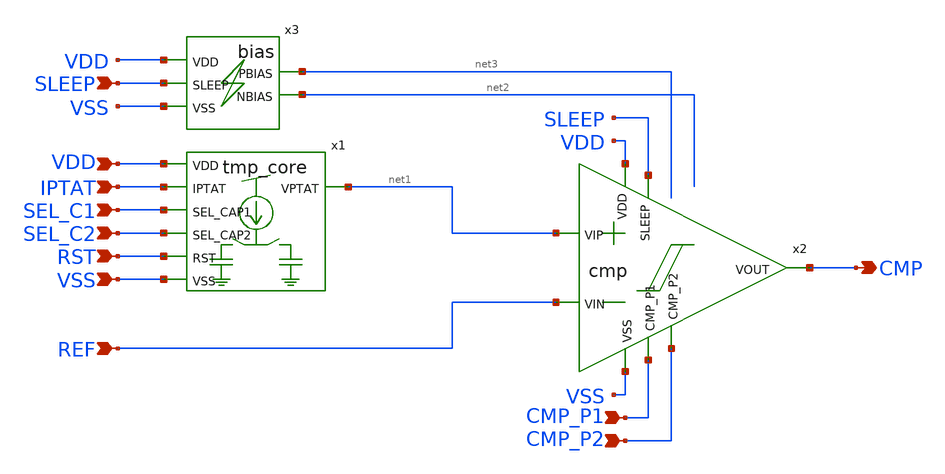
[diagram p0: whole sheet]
** sch_path: design/LELO_TORD_SKY130A/TB_tmp_core_and_cmp.sch
**.subckt TB_tmp_core_and_cmp VDD IPTAT SEL_C1 SEL_C2 RST VSS REF CMP CMP_P1 CMP_P2 SLEEP
*.ipin VDD
*.ipin IPTAT
*.ipin SEL_C1
*.ipin SEL_C2
*.ipin RST
*.ipin VSS
*.ipin REF
*.opin CMP
*.ipin CMP_P1
*.ipin CMP_P2
*.ipin SLEEP
x1 VDD IPTAT SEL_C1 SEL_C2 net1 RST VSS tmp_core
x2 CMP_P1 CMP_P2 SLEEP VDD net1 REF CMP VSS cmp
x3 VDD SLEEP VSS net3 net2 bias
**.ends
.end
